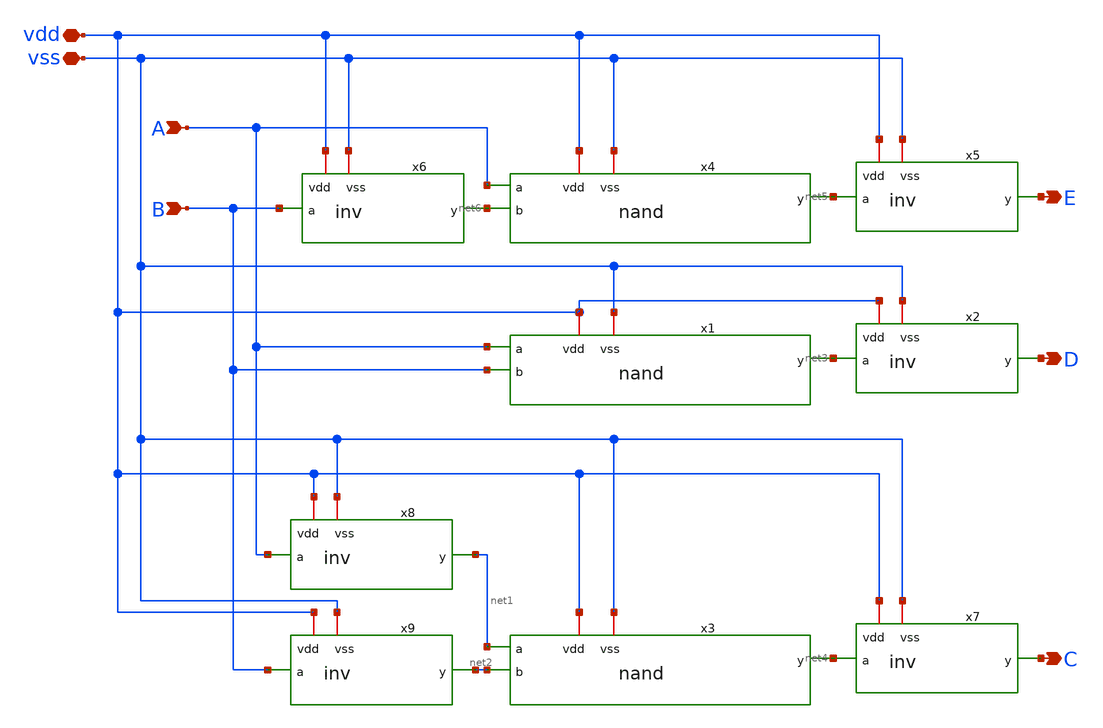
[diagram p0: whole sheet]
** sch_path: member_project/ice458/dynamic_comparator/xschem/decode.sch
**.subckt decode A B vdd vss E D C
*.ipin A
*.ipin B
*.iopin vdd
*.iopin vss
*.opin E
*.opin D
*.opin C
x1 vdd net3 A B vss nand
x2 vdd net3 D vss inv
x3 vdd net4 net1 net2 vss nand
x4 vdd net5 A net6 vss nand
x5 vdd net5 E vss inv
x6 vdd B net6 vss inv
x7 vdd net4 C vss inv
x8 vdd A net1 vss inv
x9 vdd B net2 vss inv
**.ends

* expanding   symbol:  nand.sym # of pins=5
** sym_path: member_project/ice458/dynamic_comparator/xschem/nand.sym
** sch_path: member_project/ice458/dynamic_comparator/xschem/nand.sch
.subckt nand vdd y a b vss
*.iopin vdd
*.iopin vss
*.ipin a
*.ipin b
*.opin y
XM14 y b vdd vdd pfet_03v3 L=0.28u W=1u nf=1 ad='int((nf+1)/2) * W/nf * 0.18u' as='int((nf+2)/2) * W/nf * 0.18u'
+ pd='2*int((nf+1)/2) * (W/nf + 0.18u)' ps='2*int((nf+2)/2) * (W/nf + 0.18u)' nrd='0.18u / W' nrs='0.18u / W'
+ sa=0 sb=0 sd=0 m=1
XM9 y b net1 vss nfet_03v3 L=0.28u W=0.42u nf=1 ad='int((nf+1)/2) * W/nf * 0.18u' as='int((nf+2)/2) * W/nf * 0.18u'
+ pd='2*int((nf+1)/2) * (W/nf + 0.18u)' ps='2*int((nf+2)/2) * (W/nf + 0.18u)' nrd='0.18u / W' nrs='0.18u / W'
+ sa=0 sb=0 sd=0 m=1
XM1 y a vdd vdd pfet_03v3 L=0.28u W=1u nf=1 ad='int((nf+1)/2) * W/nf * 0.18u' as='int((nf+2)/2) * W/nf * 0.18u'
+ pd='2*int((nf+1)/2) * (W/nf + 0.18u)' ps='2*int((nf+2)/2) * (W/nf + 0.18u)' nrd='0.18u / W' nrs='0.18u / W'
+ sa=0 sb=0 sd=0 m=1
XM2 net1 a vss vss nfet_03v3 L=0.28u W=0.42u nf=1 ad='int((nf+1)/2) * W/nf * 0.18u' as='int((nf+2)/2) * W/nf * 0.18u'
+ pd='2*int((nf+1)/2) * (W/nf + 0.18u)' ps='2*int((nf+2)/2) * (W/nf + 0.18u)' nrd='0.18u / W' nrs='0.18u / W'
+ sa=0 sb=0 sd=0 m=1
.ends


* expanding   symbol:  inv.sym # of pins=4
** sym_path: member_project/ice458/dynamic_comparator/xschem/inv.sym
** sch_path: member_project/ice458/dynamic_comparator/xschem/inv.sch
.subckt inv vdd a y vss
*.iopin vdd
*.iopin vss
*.ipin a
*.opin y
XM1 y a vss vss nfet_03v3 L=0.28u W=0.42u nf=1 ad='int((nf+1)/2) * W/nf * 0.18u' as='int((nf+2)/2) * W/nf * 0.18u'
+ pd='2*int((nf+1)/2) * (W/nf + 0.18u)' ps='2*int((nf+2)/2) * (W/nf + 0.18u)' nrd='0.18u / W' nrs='0.18u / W'
+ sa=0 sb=0 sd=0 m=1
XM2 y a vdd vdd pfet_03v3 L=0.28u W=1u nf=1 ad='int((nf+1)/2) * W/nf * 0.18u' as='int((nf+2)/2) * W/nf * 0.18u'
+ pd='2*int((nf+1)/2) * (W/nf + 0.18u)' ps='2*int((nf+2)/2) * (W/nf + 0.18u)' nrd='0.18u / W' nrs='0.18u / W'
+ sa=0 sb=0 sd=0 m=1
.ends

.end
